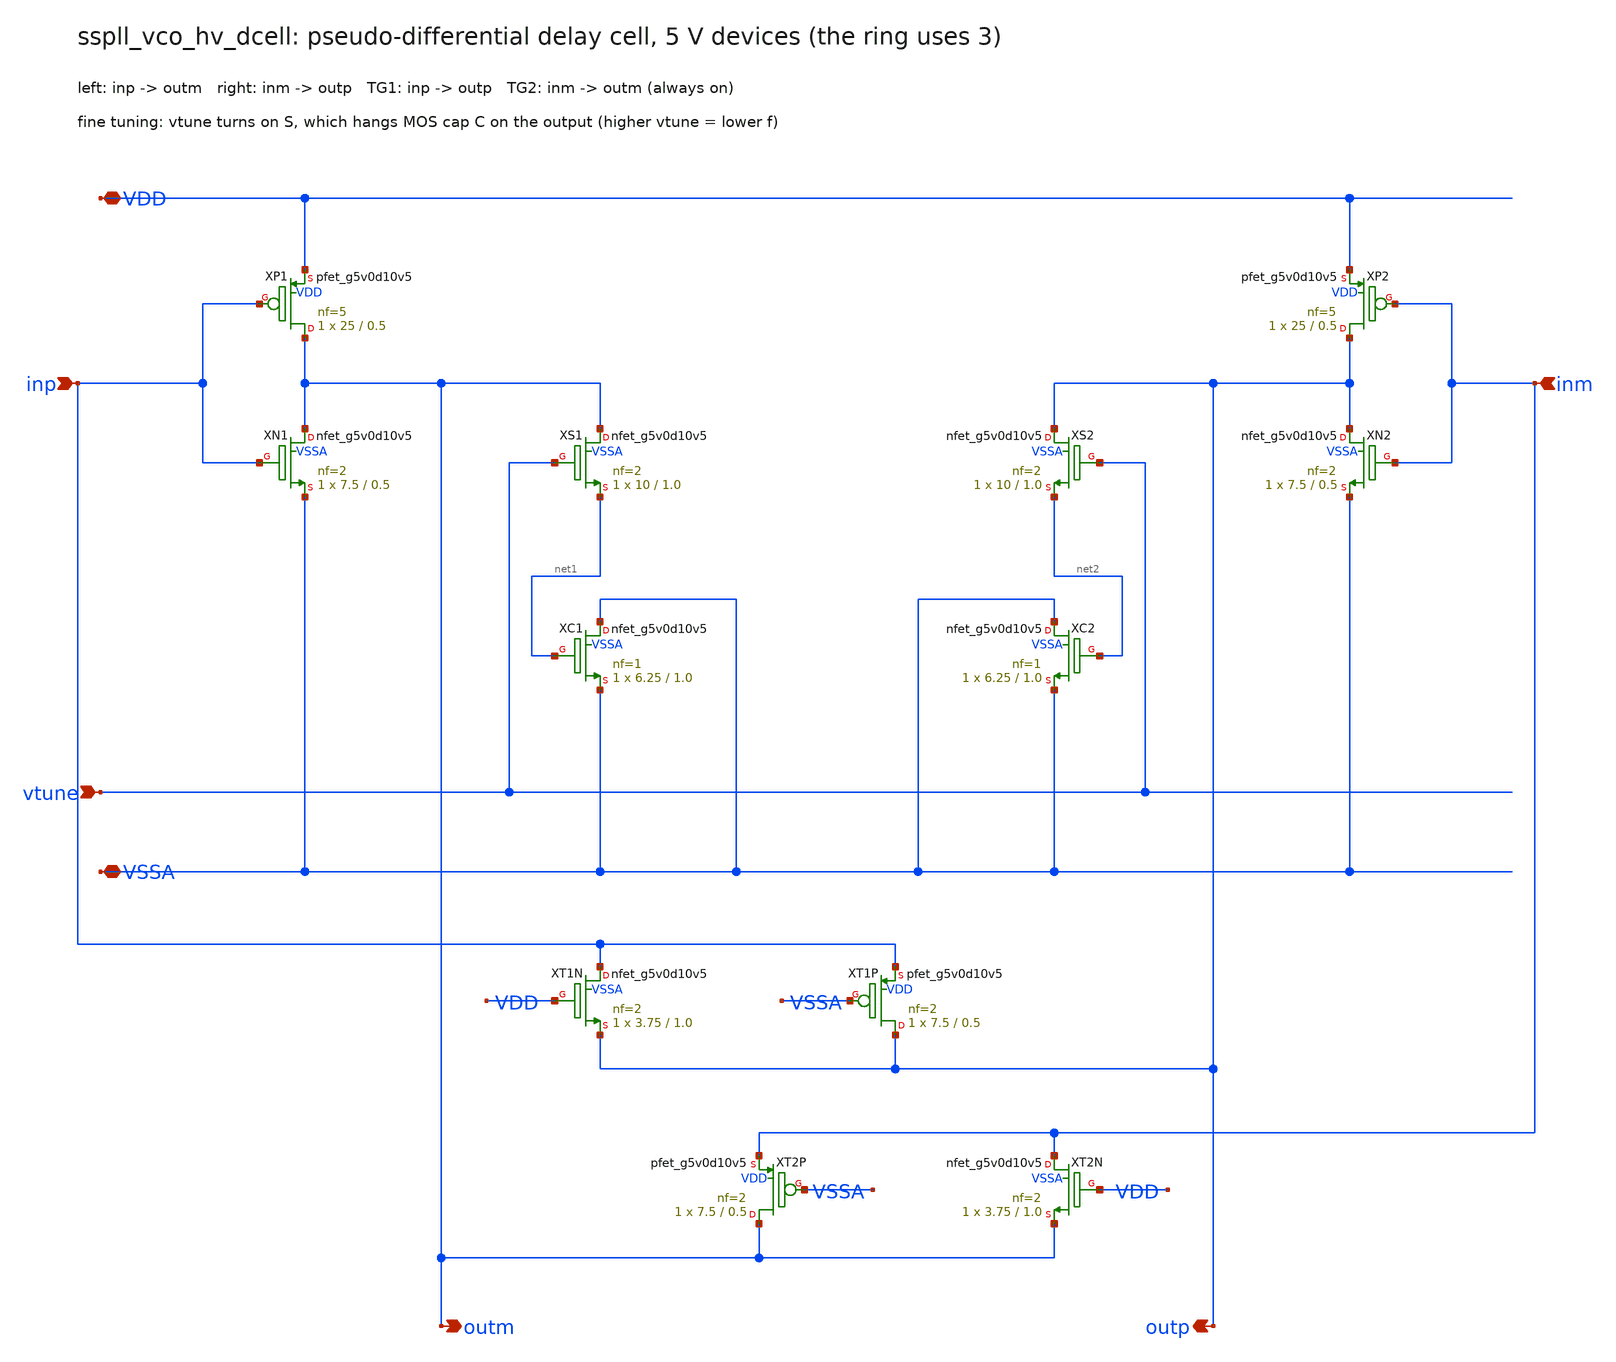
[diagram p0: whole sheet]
** sch_path: xschem/vco_hv/sspll_vco_hv_dcell.sch
**.subckt sspll_vco_hv_dcell VDD VSSA vtune inp inm outm outp
*.iopin VDD
*.iopin VSSA
*.ipin vtune
*.ipin inp
*.ipin inm
*.opin outm
*.opin outp
XXP1 outm inp VDD VDD sky130_fd_pr__pfet_g5v0d10v5 L=0.5 W=25 nf=5 ad='int((nf+1)/2) * W/nf * 0.29' as='int((nf+2)/2) * W/nf * 0.29'
+ pd='2*int((nf+1)/2) * (W/nf + 0.29)' ps='2*int((nf+2)/2) * (W/nf + 0.29)' nrd='0.29 / W' nrs='0.29 / W'
+ sa=0 sb=0 sd=0 mult=1 m=1
XXN1 outm inp VSSA VSSA sky130_fd_pr__nfet_g5v0d10v5 L=0.5 W=7.5 nf=2 ad='int((nf+1)/2) * W/nf * 0.29'
+ as='int((nf+2)/2) * W/nf * 0.29' pd='2*int((nf+1)/2) * (W/nf + 0.29)' ps='2*int((nf+2)/2) * (W/nf + 0.29)'
+ nrd='0.29 / W' nrs='0.29 / W' sa=0 sb=0 sd=0 mult=1 m=1
XXS1 outm vtune net1 VSSA sky130_fd_pr__nfet_g5v0d10v5 L=1.0 W=10 nf=2 ad='int((nf+1)/2) * W/nf * 0.29'
+ as='int((nf+2)/2) * W/nf * 0.29' pd='2*int((nf+1)/2) * (W/nf + 0.29)' ps='2*int((nf+2)/2) * (W/nf + 0.29)'
+ nrd='0.29 / W' nrs='0.29 / W' sa=0 sb=0 sd=0 mult=1 m=1
XXC1 VSSA net1 VSSA VSSA sky130_fd_pr__nfet_g5v0d10v5 L=1.0 W=6.25 nf=1 ad='int((nf+1)/2) * W/nf * 0.29'
+ as='int((nf+2)/2) * W/nf * 0.29' pd='2*int((nf+1)/2) * (W/nf + 0.29)' ps='2*int((nf+2)/2) * (W/nf + 0.29)'
+ nrd='0.29 / W' nrs='0.29 / W' sa=0 sb=0 sd=0 mult=1 m=1
XXP2 outp inm VDD VDD sky130_fd_pr__pfet_g5v0d10v5 L=0.5 W=25 nf=5 ad='int((nf+1)/2) * W/nf * 0.29' as='int((nf+2)/2) * W/nf * 0.29'
+ pd='2*int((nf+1)/2) * (W/nf + 0.29)' ps='2*int((nf+2)/2) * (W/nf + 0.29)' nrd='0.29 / W' nrs='0.29 / W'
+ sa=0 sb=0 sd=0 mult=1 m=1
XXN2 outp inm VSSA VSSA sky130_fd_pr__nfet_g5v0d10v5 L=0.5 W=7.5 nf=2 ad='int((nf+1)/2) * W/nf * 0.29'
+ as='int((nf+2)/2) * W/nf * 0.29' pd='2*int((nf+1)/2) * (W/nf + 0.29)' ps='2*int((nf+2)/2) * (W/nf + 0.29)'
+ nrd='0.29 / W' nrs='0.29 / W' sa=0 sb=0 sd=0 mult=1 m=1
XXS2 outp vtune net2 VSSA sky130_fd_pr__nfet_g5v0d10v5 L=1.0 W=10 nf=2 ad='int((nf+1)/2) * W/nf * 0.29'
+ as='int((nf+2)/2) * W/nf * 0.29' pd='2*int((nf+1)/2) * (W/nf + 0.29)' ps='2*int((nf+2)/2) * (W/nf + 0.29)'
+ nrd='0.29 / W' nrs='0.29 / W' sa=0 sb=0 sd=0 mult=1 m=1
XXC2 VSSA net2 VSSA VSSA sky130_fd_pr__nfet_g5v0d10v5 L=1.0 W=6.25 nf=1 ad='int((nf+1)/2) * W/nf * 0.29'
+ as='int((nf+2)/2) * W/nf * 0.29' pd='2*int((nf+1)/2) * (W/nf + 0.29)' ps='2*int((nf+2)/2) * (W/nf + 0.29)'
+ nrd='0.29 / W' nrs='0.29 / W' sa=0 sb=0 sd=0 mult=1 m=1
XXT1N inp VDD outp VSSA sky130_fd_pr__nfet_g5v0d10v5 L=1.0 W=3.75 nf=2 ad='int((nf+1)/2) * W/nf * 0.29'
+ as='int((nf+2)/2) * W/nf * 0.29' pd='2*int((nf+1)/2) * (W/nf + 0.29)' ps='2*int((nf+2)/2) * (W/nf + 0.29)'
+ nrd='0.29 / W' nrs='0.29 / W' sa=0 sb=0 sd=0 mult=1 m=1
XXT1P outp VSSA inp VDD sky130_fd_pr__pfet_g5v0d10v5 L=0.5 W=7.5 nf=2 ad='int((nf+1)/2) * W/nf * 0.29'
+ as='int((nf+2)/2) * W/nf * 0.29' pd='2*int((nf+1)/2) * (W/nf + 0.29)' ps='2*int((nf+2)/2) * (W/nf + 0.29)'
+ nrd='0.29 / W' nrs='0.29 / W' sa=0 sb=0 sd=0 mult=1 m=1
XXT2N inm VDD outm VSSA sky130_fd_pr__nfet_g5v0d10v5 L=1.0 W=3.75 nf=2 ad='int((nf+1)/2) * W/nf * 0.29'
+ as='int((nf+2)/2) * W/nf * 0.29' pd='2*int((nf+1)/2) * (W/nf + 0.29)' ps='2*int((nf+2)/2) * (W/nf + 0.29)'
+ nrd='0.29 / W' nrs='0.29 / W' sa=0 sb=0 sd=0 mult=1 m=1
XXT2P outm VSSA inm VDD sky130_fd_pr__pfet_g5v0d10v5 L=0.5 W=7.5 nf=2 ad='int((nf+1)/2) * W/nf * 0.29'
+ as='int((nf+2)/2) * W/nf * 0.29' pd='2*int((nf+1)/2) * (W/nf + 0.29)' ps='2*int((nf+2)/2) * (W/nf + 0.29)'
+ nrd='0.29 / W' nrs='0.29 / W' sa=0 sb=0 sd=0 mult=1 m=1
**.ends
.end
